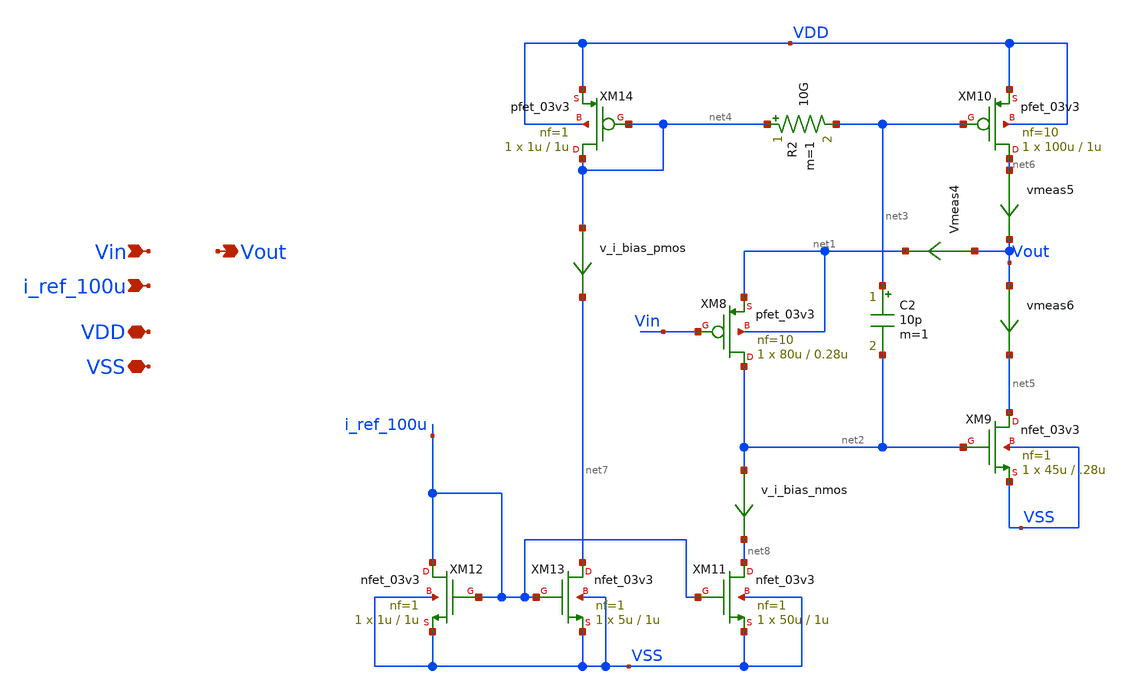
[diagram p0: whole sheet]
** sch_path: designs/output_buffer/schematic/output_buffer_pfet_input.sch
**.subckt output_buffer_pfet_input Vin Vout i_ref_100u VDD VSS
*.ipin Vin
*.opin Vout
*.ipin i_ref_100u
*.iopin VDD
*.iopin VSS
XM8 net2 Vin net1 net1 pfet_03v3 L=0.28u W=80u nf=10 ad='int((nf+1)/2) * W/nf * 0.18u' as='int((nf+2)/2) * W/nf * 0.18u'
+ pd='2*int((nf+1)/2) * (W/nf + 0.18u)' ps='2*int((nf+2)/2) * (W/nf + 0.18u)' nrd='0.18u / W' nrs='0.18u / W'
+ sa=0 sb=0 sd=0 m=1
XM9 net5 net2 VSS VSS nfet_03v3 L=.28u W=45u nf=1 ad='int((nf+1)/2) * W/nf * 0.18u' as='int((nf+2)/2) * W/nf * 0.18u'
+ pd='2*int((nf+1)/2) * (W/nf + 0.18u)' ps='2*int((nf+2)/2) * (W/nf + 0.18u)' nrd='0.18u / W' nrs='0.18u / W'
+ sa=0 sb=0 sd=0 m=1
C2 net3 net2 10p m=1
XM10 net6 net3 VDD VDD pfet_03v3 L=1u W=100u nf=10 ad='int((nf+1)/2) * W/nf * 0.18u' as='int((nf+2)/2) * W/nf * 0.18u'
+ pd='2*int((nf+1)/2) * (W/nf + 0.18u)' ps='2*int((nf+2)/2) * (W/nf + 0.18u)' nrd='0.18u / W' nrs='0.18u / W'
+ sa=0 sb=0 sd=0 m=1
R2 net4 net3 10G m=1
XM11 net8 i_ref_100u VSS VSS nfet_03v3 L=1u W=50u nf=1 ad='int((nf+1)/2) * W/nf * 0.18u' as='int((nf+2)/2) * W/nf * 0.18u'
+ pd='2*int((nf+1)/2) * (W/nf + 0.18u)' ps='2*int((nf+2)/2) * (W/nf + 0.18u)' nrd='0.18u / W' nrs='0.18u / W'
+ sa=0 sb=0 sd=0 m=1
XM12 i_ref_100u i_ref_100u VSS VSS nfet_03v3 L=1u W=1u nf=1 ad='int((nf+1)/2) * W/nf * 0.18u' as='int((nf+2)/2) * W/nf * 0.18u'
+ pd='2*int((nf+1)/2) * (W/nf + 0.18u)' ps='2*int((nf+2)/2) * (W/nf + 0.18u)' nrd='0.18u / W' nrs='0.18u / W'
+ sa=0 sb=0 sd=0 m=1
XM13 net7 i_ref_100u VSS VSS nfet_03v3 L=1u W=5u nf=1 ad='int((nf+1)/2) * W/nf * 0.18u' as='int((nf+2)/2) * W/nf * 0.18u'
+ pd='2*int((nf+1)/2) * (W/nf + 0.18u)' ps='2*int((nf+2)/2) * (W/nf + 0.18u)' nrd='0.18u / W' nrs='0.18u / W'
+ sa=0 sb=0 sd=0 m=1
XM14 net4 net4 VDD VDD pfet_03v3 L=1u W=1u nf=1 ad='int((nf+1)/2) * W/nf * 0.18u' as='int((nf+2)/2) * W/nf * 0.18u'
+ pd='2*int((nf+1)/2) * (W/nf + 0.18u)' ps='2*int((nf+2)/2) * (W/nf + 0.18u)' nrd='0.18u / W' nrs='0.18u / W'
+ sa=0 sb=0 sd=0 m=1
Vmeas4 Vout net1 0
.save i(vmeas4)
vmeas5 net6 Vout 0
.save i(vmeas5)
vmeas6 Vout net5 0
.save i(vmeas6)
v_i_bias_pmos net4 net7 0
.save i(v_i_bias_pmos)
v_i_bias_nmos net2 net8 0
.save i(v_i_bias_nmos)
**.ends
.end
